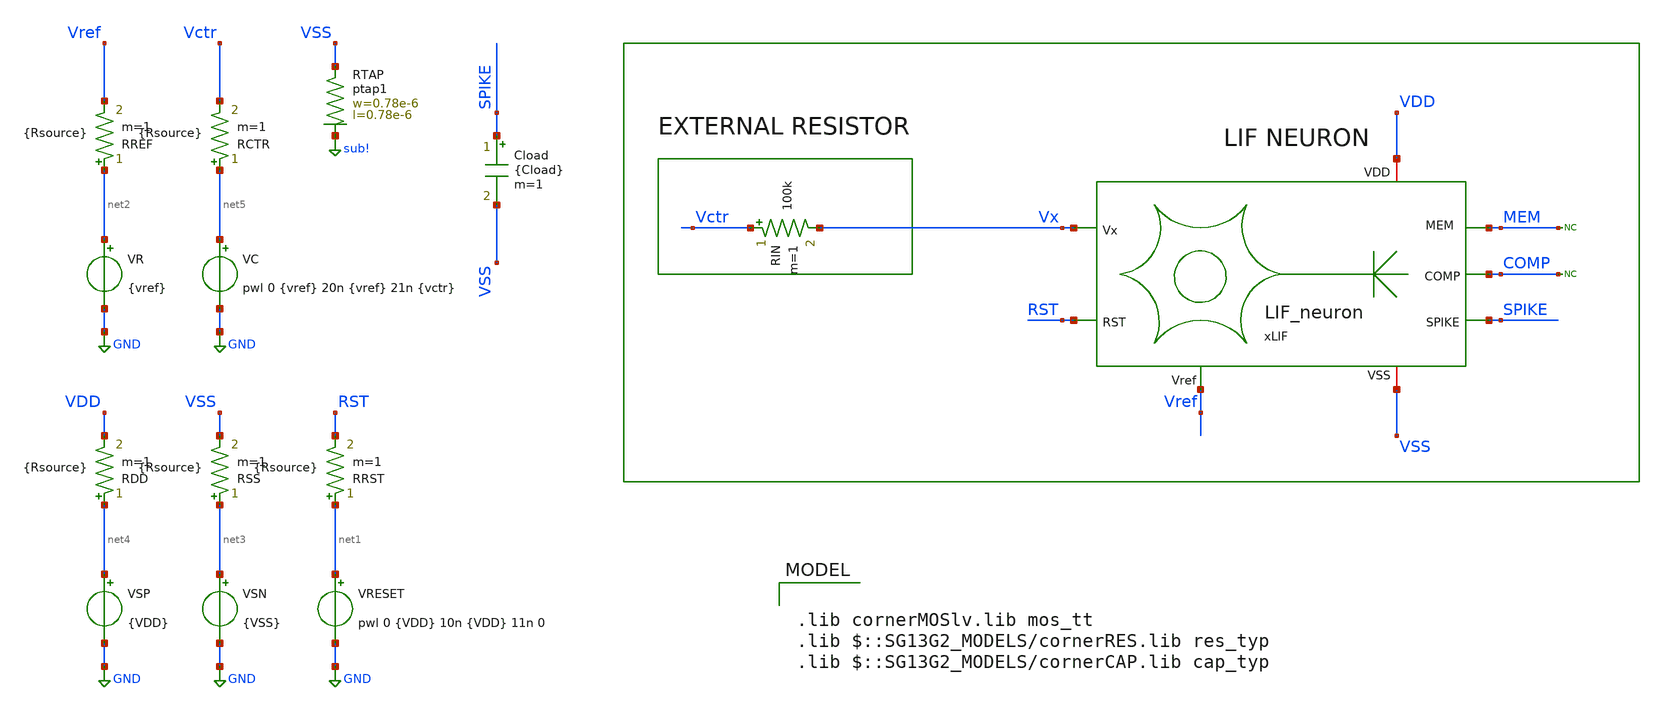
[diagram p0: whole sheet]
** sch_path: work/LIF_neuron/xschem/sweep_espk_LIF_neuron.sch
**.subckt sweep_espk_LIF_neuron
VRESET net1 GND pwl 0 {VDD} 10n {VDD} 11n 0
VSN net3 GND {VSS}
VR net2 GND {vref}
VC net5 GND pwl 0 {vref} 20n {vref} 21n {vctr}
RDD net4 VDD {Rsource} m=1
RSS net3 VSS {Rsource} m=1
RRST net1 RST {Rsource} m=1
RREF net2 Vref {Rsource} m=1
RCTR net5 Vctr {Rsource} m=1
Cload SPIKE VSS {Cload} m=1
RIN Vctr Vx 100k m=1
VSP net4 GND {VDD}
* noconn MEM
XRTAP VSS sub! ptap1 R=262.8 w=0.78e-6 l=0.78e-6
xLIF VDD Vx MEM RST SPIKE VSS Vref COMP LIF_neuron
* noconn COMP
**** begin user architecture code



.param VDD = 1.2
.param VSS = 0
.param vctr = 0.6
.param vref = 1.2
.param Cload = 0.1p
.param Rsource = 1m

.param sw_stat_global = 0
.param sw_stat_mismatch = 0

.save all

.control

* >> Variables <<

let tstop = 0.1u
let tstep = tstop/2.5k

=====================barrido===================

let VDD_start = 0
let VDD_end   = 1.2
let VDD_step  = 0.03

let idx = 0

let npoints = (VDD_end - VDD_start)/VDD_step

====================vectores===================

let VDD_vec = vector(npoints)
let Vhigh_vec = vector(npoints)
let Vmid_vec = vector(npoints)
let spike_vec = vector(npoints)
let IDD_vec = vector(npoints)
let idd_avg_vec = vector(npoints)
let P_avg_vec = vector(npoints)
let F_spk_vec = vector(npoints)
let E_spk_vec = vector(npoints)

settype voltage VDD_vec
settype voltage Vhigh_vec
settype voltage Vmid_vec
settype voltage spike_vec
settype current IDD_vec
settype current idd_avg_vec
settype power P_avg_vec
settype frequency F_spk_vec
settype energy E_spk_vec

===============================================

let v = VDD_start

while v le VDD_end

  alterparam VDD = $&v

  reset

  tran $&tstep $&tstop

  meas tran SPIKE_max max v(SPIKE)

  let spike_vec[idx] = SPIKE_max

  let Vmid_vec[idx] = v * 0.5

  meas tran idd_avg AVG i(VSP) from=tstep to=tstop

  let IDD_vec[idx] = abs(idd_avg)

  let P_avg_vec[idx] = abs(v*IDD_vec[idx])

  meas TRAN T_spk TRIG v(SPIKE) VAL=(v*0.5) rise=2 TARG v(SPIKE) VAL=(v*0.5) rise=3

  let F_spk_vec[idx] = 1 / T_spk

  if (F_spk_vec[idx] < 1k)

      let E_spk_vec[idx] = 0

  else

      let E_spk_vec[idx] = P_avg_vec[idx]/F_spk_vec[idx]

  end

  let VDD_vec[idx] = v

  let v = v + VDD_step

  let idx = idx + 1

end

print v(VDD_vec) IDD_vec P_avg_vec v(spike_vec) E_spk_vec F_spk_vec


plot spike_vec vs VDD_vec
plot E_spk_vec vs VDD_vec
plot F_spk_vec vs VDD_vec
plot P_avg_vec vs VDD_vec


setplot const
setscale VDD_vec

set wr_vcnames
option numdgt=6
wrdata /foss/designs/chipathon_2025/designs/ihp-sg13g2/LIF_neuron/xschem/resultados.txt VDD_vec
+ spike_vec E_spk_vec  F_spk_vec P_avg_vec


.endc



.lib cornerMOSlv.lib mos_tt
.lib $::SG13G2_MODELS/cornerRES.lib res_typ
.lib $::SG13G2_MODELS/cornerCAP.lib cap_typ

**** end user architecture code
**.ends
.GLOBAL GND
.GLOBAL sub!
.end
